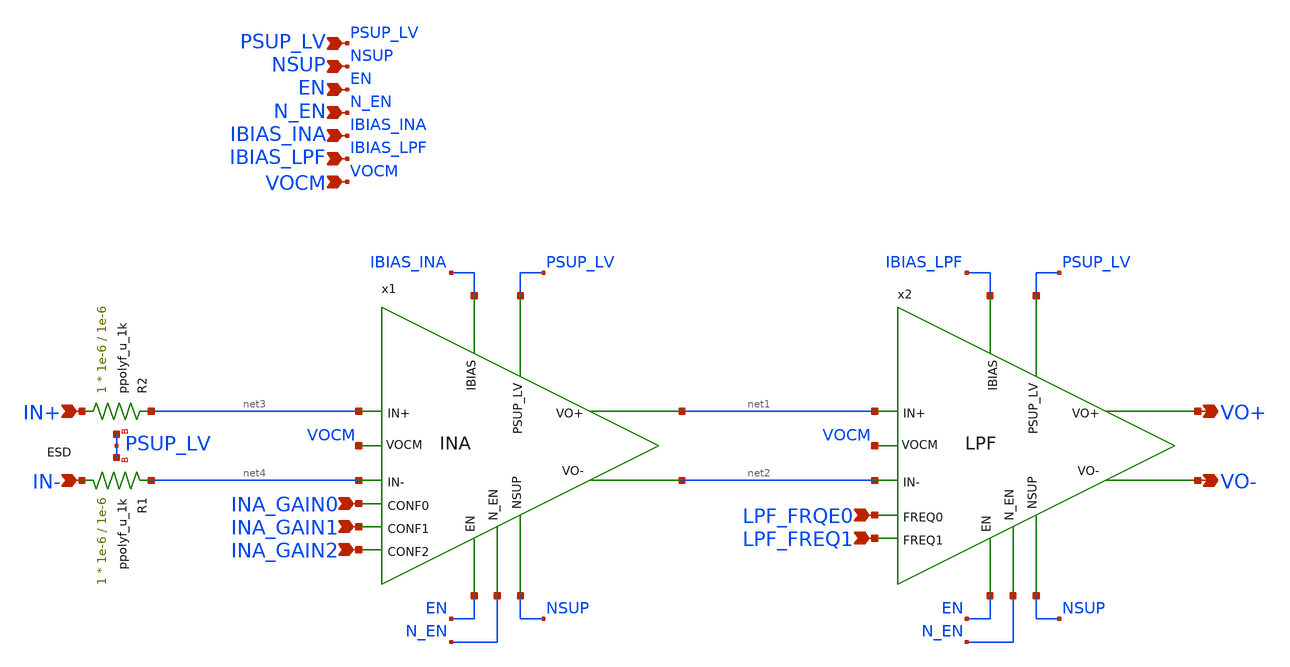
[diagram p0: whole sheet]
** sch_path: xschem/top.sch
**.subckt top IN+ IN- EN N_EN NSUP PSUP_LV IBIAS_INA VOCM VO+ VO- LPF_FREQ1 LPF_FRQE0 INA_GAIN1
*+ INA_GAIN0 IBIAS_LPF INA_GAIN2
*.ipin IN+
*.ipin IN-
*.ipin EN
*.ipin N_EN
*.ipin NSUP
*.ipin PSUP_LV
*.ipin IBIAS_INA
*.ipin VOCM
*.opin VO+
*.opin VO-
*.ipin LPF_FREQ1
*.ipin LPF_FRQE0
*.ipin INA_GAIN1
*.ipin INA_GAIN0
*.ipin IBIAS_LPF
*.ipin INA_GAIN2
x2 PSUP_LV NSUP EN N_EN IBIAS_LPF LPF_FREQ1 LPF_FRQE0 net1 VO+ VOCM net2 VO- LPF
x1 PSUP_LV NSUP EN N_EN IBIAS_INA INA_GAIN0 INA_GAIN1 net3 net1 VOCM net4 net2 INA_GAIN2 INA
XR2 IN+ net3 PSUP_LV ppolyf_u_1k r_width=1e-6 r_length=1e-6 m=1
XR1 IN- net4 PSUP_LV ppolyf_u_1k r_width=1e-6 r_length=1e-6 m=1
**.ends
.end
